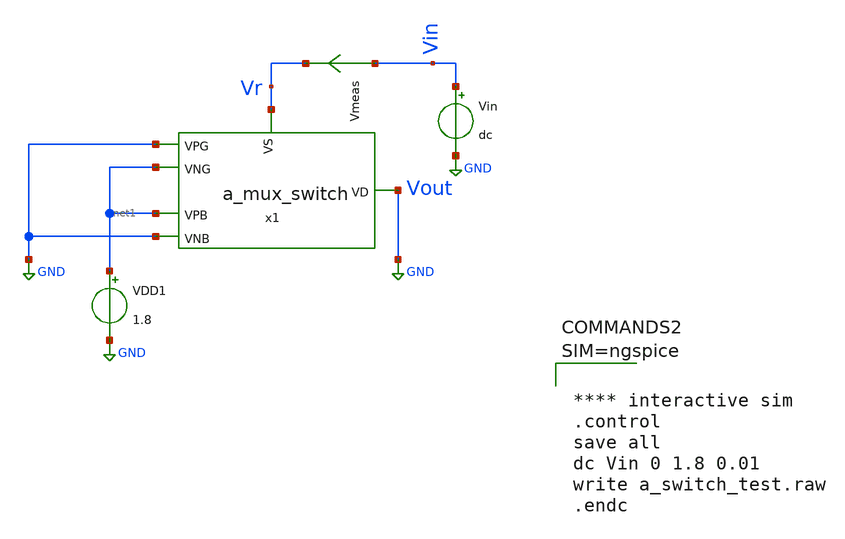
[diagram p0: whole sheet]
** sch_path: a_switch_test.sch
**.subckt a_switch_test
VDD1 net1 GND 1.8
Vin Vin GND dc
x1 GND net1 net1 GND Vr Vout a_mux_switch
Vmeas Vin Vr 0
.save i(vmeas)
**** begin user architecture code

** opencircuitdesign pdks install
.lib $::SKYWATER_MODELS/sky130.lib.spice tt
.include $::SKYWATER_STDCELLS/sky130_fd_sc_hd.spice





**** interactive sim
.control
save all
dc Vin 0 1.8 0.01
write a_switch_test.raw
.endc



**** end user architecture code
**.ends

* expanding   symbol:  analog_mux_files 2/a_mux_switch.sym # of pins=6
** sym_path: analog_mux_files 2/a_mux_switch.sym
** sch_path: analog_mux_files 2/a_mux_switch.sch
.subckt a_mux_switch VNB VNG VPB VPG VS VD
*.ipin VPG
*.ipin VNG
*.ipin VS
*.opin VD
*.ipin VPB
*.ipin VNB
XM1 VD VPG VS VPB sky130_fd_pr__pfet_01v8 L=0.15 W=20 nf=1 ad='int((nf+1)/2) * W/nf * 0.29' as='int((nf+2)/2) * W/nf * 0.29'
+ pd='2*int((nf+1)/2) * (W/nf + 0.29)' ps='2*int((nf+2)/2) * (W/nf + 0.29)' nrd='0.29 / W' nrs='0.29 / W'
+ sa=0 sb=0 sd=0 mult=1 m=1
XM2 VD VNG VS VNB sky130_fd_pr__nfet_01v8 L=0.15 W=20 nf=1 ad='int((nf+1)/2) * W/nf * 0.29' as='int((nf+2)/2) * W/nf * 0.29'
+ pd='2*int((nf+1)/2) * (W/nf + 0.29)' ps='2*int((nf+2)/2) * (W/nf + 0.29)' nrd='0.29 / W' nrs='0.29 / W'
+ sa=0 sb=0 sd=0 mult=1 m=1
.ends

.GLOBAL GND
.end
